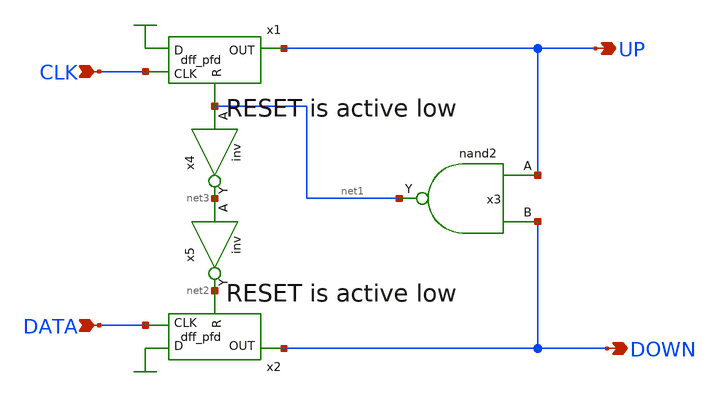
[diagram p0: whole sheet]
** sch_path: pfd.sch
**.subckt pfd DATA CLK UP DOWN
*.ipin DATA
*.ipin CLK
*.opin UP
*.opin DOWN
x1 UP CLK net1 dff_pfd
x2 DOWN DATA net2 dff_pfd
x3 UP DOWN net1 nand2
x4 net1 net3 inv
x5 net3 net2 inv
**.ends

* expanding   symbol:  dff_pfd.sym # of pins=3
** sym_path: dff_pfd.sym
** sch_path: dff_pfd.sch
.subckt dff_pfd OUT CLK R
*.opin OUT
*.ipin R
*.ipin CLK
x1 net2 net4 net5 nand2
x2 net5 CLK R net4 nand3
x4 net4 CLK net2 net1 nand3
x5 net4 net3 OUT nand2
x6 OUT net1 R net3 nand3
x3 net1 R net2 nand2
.ends


* expanding   symbol:  nand2.sym # of pins=3
** sym_path: nand2.sym
** sch_path: nand2.sch
.subckt nand2 A B Y
*.ipin B
*.ipin A
*.opin Y
XM29 Y B VDD VDD pfet_06v0 L=0.50u W=2u nf=1 ad='int((nf+1)/2) * W/nf * 0.18u' as='int((nf+2)/2) * W/nf * 0.18u'
+ pd='2*int((nf+1)/2) * (W/nf + 0.18u)' ps='2*int((nf+2)/2) * (W/nf + 0.18u)' nrd='0.18u / W' nrs='0.18u / W'
+ sa=0 sb=0 sd=0 m=1
XM30 Y A VDD VDD pfet_06v0 L=0.50u W=2u nf=1 ad='int((nf+1)/2) * W/nf * 0.18u' as='int((nf+2)/2) * W/nf * 0.18u'
+ pd='2*int((nf+1)/2) * (W/nf + 0.18u)' ps='2*int((nf+2)/2) * (W/nf + 0.18u)' nrd='0.18u / W' nrs='0.18u / W'
+ sa=0 sb=0 sd=0 m=1
XM31 Y A net1 GND nfet_06v0 L=0.60u W=0.9u nf=1 ad='int((nf+1)/2) * W/nf * 0.18u' as='int((nf+2)/2) * W/nf * 0.18u'
+ pd='2*int((nf+1)/2) * (W/nf + 0.18u)' ps='2*int((nf+2)/2) * (W/nf + 0.18u)' nrd='0.18u / W' nrs='0.18u / W'
+ sa=0 sb=0 sd=0 m=1
XM32 net1 B GND GND nfet_06v0 L=0.60u W=0.9u nf=1 ad='int((nf+1)/2) * W/nf * 0.18u' as='int((nf+2)/2) * W/nf * 0.18u'
+ pd='2*int((nf+1)/2) * (W/nf + 0.18u)' ps='2*int((nf+2)/2) * (W/nf + 0.18u)' nrd='0.18u / W' nrs='0.18u / W'
+ sa=0 sb=0 sd=0 m=1
.ends


* expanding   symbol:  inv.sym # of pins=2
** sym_path: inv.sym
** sch_path: inv.sch
.subckt inv A Y
*.opin Y
*.ipin A
XM1 Y A VDD VDD pfet_06v0 L=0.50u W=2u nf=1 ad='int((nf+1)/2) * W/nf * 0.18u' as='int((nf+2)/2) * W/nf * 0.18u'
+ pd='2*int((nf+1)/2) * (W/nf + 0.18u)' ps='2*int((nf+2)/2) * (W/nf + 0.18u)' nrd='0.18u / W' nrs='0.18u / W'
+ sa=0 sb=0 sd=0 m=1
XM2 Y A GND GND nfet_06v0 L=0.60u W=0.9u nf=1 ad='int((nf+1)/2) * W/nf * 0.18u' as='int((nf+2)/2) * W/nf * 0.18u'
+ pd='2*int((nf+1)/2) * (W/nf + 0.18u)' ps='2*int((nf+2)/2) * (W/nf + 0.18u)' nrd='0.18u / W' nrs='0.18u / W'
+ sa=0 sb=0 sd=0 m=1
.ends


* expanding   symbol:  nand3.sym # of pins=4
** sym_path: nand3.sym
** sch_path: nand3.sch
.subckt nand3 A B C Y
*.ipin B
*.ipin A
*.opin Y
*.ipin C
XM3 Y B VDD VDD pfet_06v0 L=0.50u W=2u nf=1 ad='int((nf+1)/2) * W/nf * 0.18u' as='int((nf+2)/2) * W/nf * 0.18u'
+ pd='2*int((nf+1)/2) * (W/nf + 0.18u)' ps='2*int((nf+2)/2) * (W/nf + 0.18u)' nrd='0.18u / W' nrs='0.18u / W'
+ sa=0 sb=0 sd=0 m=1
XM1 Y A VDD VDD pfet_06v0 L=0.50u W=2u nf=1 ad='int((nf+1)/2) * W/nf * 0.18u' as='int((nf+2)/2) * W/nf * 0.18u'
+ pd='2*int((nf+1)/2) * (W/nf + 0.18u)' ps='2*int((nf+2)/2) * (W/nf + 0.18u)' nrd='0.18u / W' nrs='0.18u / W'
+ sa=0 sb=0 sd=0 m=1
XM2 Y A net1 GND nfet_06v0 L=0.60u W=0.9u nf=1 ad='int((nf+1)/2) * W/nf * 0.18u' as='int((nf+2)/2) * W/nf * 0.18u'
+ pd='2*int((nf+1)/2) * (W/nf + 0.18u)' ps='2*int((nf+2)/2) * (W/nf + 0.18u)' nrd='0.18u / W' nrs='0.18u / W'
+ sa=0 sb=0 sd=0 m=1
XM4 net1 B net2 GND nfet_06v0 L=0.60u W=0.9u nf=1 ad='int((nf+1)/2) * W/nf * 0.18u' as='int((nf+2)/2) * W/nf * 0.18u'
+ pd='2*int((nf+1)/2) * (W/nf + 0.18u)' ps='2*int((nf+2)/2) * (W/nf + 0.18u)' nrd='0.18u / W' nrs='0.18u / W'
+ sa=0 sb=0 sd=0 m=1
XM5 Y C VDD VDD pfet_06v0 L=0.50u W=2u nf=1 ad='int((nf+1)/2) * W/nf * 0.18u' as='int((nf+2)/2) * W/nf * 0.18u'
+ pd='2*int((nf+1)/2) * (W/nf + 0.18u)' ps='2*int((nf+2)/2) * (W/nf + 0.18u)' nrd='0.18u / W' nrs='0.18u / W'
+ sa=0 sb=0 sd=0 m=1
XM6 net2 C GND GND nfet_06v0 L=0.60u W=0.9u nf=1 ad='int((nf+1)/2) * W/nf * 0.18u' as='int((nf+2)/2) * W/nf * 0.18u'
+ pd='2*int((nf+1)/2) * (W/nf + 0.18u)' ps='2*int((nf+2)/2) * (W/nf + 0.18u)' nrd='0.18u / W' nrs='0.18u / W'
+ sa=0 sb=0 sd=0 m=1
.ends

.GLOBAL VDD
.GLOBAL GND
.end
